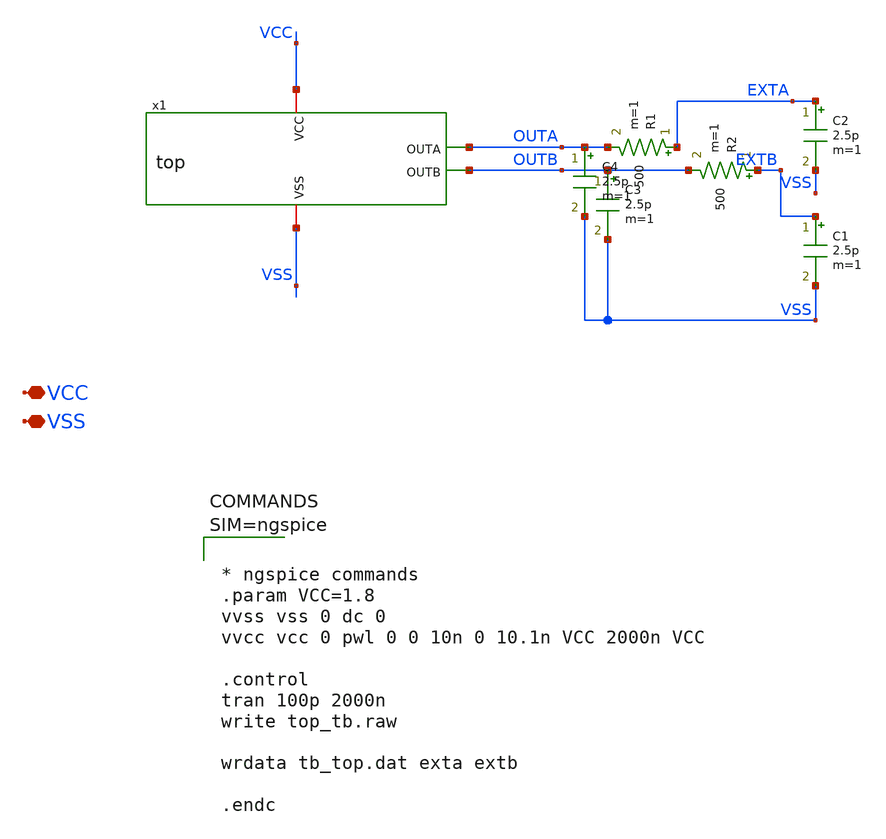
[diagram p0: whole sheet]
** sch_path: xschem/top_tb.sch
**.subckt top_tb VCC VSS
*.iopin VCC
*.iopin VSS
x1 VCC OUTA OUTB VSS top
R1 EXTA OUTA 500 m=1
R2 EXTB OUTB 500 m=1
C1 EXTB VSS 2.5p m=1
C2 EXTA VSS 2.5p m=1
C3 OUTB VSS 2.5p m=1
C4 OUTA VSS 2.5p m=1
**** begin user architecture code

** opencircuitdesign pdks install
.lib $::SKYWATER_MODELS/sky130.lib.spice tt





* ngspice commands
.param VCC=1.8
vvss vss 0 dc 0
vvcc vcc 0 pwl 0 0 10n 0 10.1n VCC 2000n VCC

.control
tran 100p 2000n
write top_tb.raw

wrdata tb_top.dat exta extb

.endc




**** end user architecture code
**.ends

* expanding   symbol:  top.sym # of pins=4
** sym_path: xschem/top.sym
** sch_path: xschem/top.sch
.subckt top VCC OUTA OUTB VSS
*.iopin VCC
*.iopin VSS
*.opin OUTA
*.opin OUTB
x1 VCC OSCA VSS oscillator_20MHZ
x2 VCC OSCB VSS oscillator_21MHZ
x5 VCC VSS IBIAS current_source
x6 VCC FIL_OUTA OSCA_BUF VSS IBIAS filter22M
x7 VCC FIL_OUTB OSCB_BUF VSS IBIAS filter22M
x10 VCC OSCA OSCA_BUF IBIAS VSS analog_buffer
x8 VCC OSCB OSCB_BUF IBIAS VSS analog_buffer
x9 VCC FIL_OUTA OUTA IBIAS VSS analog_buffer
x3 VCC FIL_OUTB OUTB IBIAS VSS analog_buffer
.ends


* expanding   symbol:  oscillator_20MHZ.sym # of pins=3
** sym_path: xschem/oscillator_20MHZ.sym
** sch_path: xschem/oscillator_20MHZ.sch
.subckt oscillator_20MHZ VCC OUT VSS
*.iopin VCC
*.iopin VSS
*.opin OUT
x1[30] INI[29] OUT_INI VCC VSS inverter
x1[29] INI[28] INI[29] VCC VSS inverter
x1[28] INI[27] INI[28] VCC VSS inverter
x1[27] INI[26] INI[27] VCC VSS inverter
x1[26] INI[25] INI[26] VCC VSS inverter
x1[25] INI[24] INI[25] VCC VSS inverter
x1[24] INI[23] INI[24] VCC VSS inverter
x1[23] INI[22] INI[23] VCC VSS inverter
x1[22] INI[21] INI[22] VCC VSS inverter
x1[21] INI[20] INI[21] VCC VSS inverter
x1[20] INI[19] INI[20] VCC VSS inverter
x1[19] INI[18] INI[19] VCC VSS inverter
x1[18] INI[17] INI[18] VCC VSS inverter
x1[17] INI[16] INI[17] VCC VSS inverter
x1[16] INI[15] INI[16] VCC VSS inverter
x1[15] INI[14] INI[15] VCC VSS inverter
x1[14] INI[13] INI[14] VCC VSS inverter
x1[13] INI[12] INI[13] VCC VSS inverter
x1[12] INI[11] INI[12] VCC VSS inverter
x1[11] INI[10] INI[11] VCC VSS inverter
x1[10] INI[9] INI[10] VCC VSS inverter
x1[9] INI[8] INI[9] VCC VSS inverter
x1[8] INI[7] INI[8] VCC VSS inverter
x1[7] INI[6] INI[7] VCC VSS inverter
x1[6] INI[5] INI[6] VCC VSS inverter
x1[5] INI[4] INI[5] VCC VSS inverter
x1[4] INI[3] INI[4] VCC VSS inverter
x1[3] INI[2] INI[3] VCC VSS inverter
x1[2] INI[1] INI[2] VCC VSS inverter
x1[1] INI[0] INI[1] VCC VSS inverter
x1[0] OUT_INI INI[0] VCC VSS inverter
x3 OUT OUT_INI VCC VSS inverter
.ends


* expanding   symbol:  oscillator_21MHZ.sym # of pins=3
** sym_path: xschem/oscillator_21MHZ.sym
** sch_path: xschem/oscillator_21MHZ.sch
.subckt oscillator_21MHZ VCC OUT VSS
*.iopin VCC
*.iopin VSS
*.opin OUT
x1[20] INI[19] OUT_INI VCC VSS inverter
x1[19] INI[18] INI[19] VCC VSS inverter
x1[18] INI[17] INI[18] VCC VSS inverter
x1[17] INI[16] INI[17] VCC VSS inverter
x1[16] INI[15] INI[16] VCC VSS inverter
x1[15] INI[14] INI[15] VCC VSS inverter
x1[14] INI[13] INI[14] VCC VSS inverter
x1[13] INI[12] INI[13] VCC VSS inverter
x1[12] INI[11] INI[12] VCC VSS inverter
x1[11] INI[10] INI[11] VCC VSS inverter
x1[10] INI[9] INI[10] VCC VSS inverter
x1[9] INI[8] INI[9] VCC VSS inverter
x1[8] INI[7] INI[8] VCC VSS inverter
x1[7] INI[6] INI[7] VCC VSS inverter
x1[6] INI[5] INI[6] VCC VSS inverter
x1[5] INI[4] INI[5] VCC VSS inverter
x1[4] INI[3] INI[4] VCC VSS inverter
x1[3] INI[2] INI[3] VCC VSS inverter
x1[2] INI[1] INI[2] VCC VSS inverter
x1[1] INI[0] INI[1] VCC VSS inverter
x1[0] OUT_INI INI[0] VCC VSS inverter
x1 OUT OUT_INI VCC VSS inverter
.ends


* expanding   symbol:  current_source.sym # of pins=3
** sym_path: xschem/current_source.sym
** sch_path: xschem/current_source.sch
.subckt current_source VCC VSS IBIAS
*.iopin VCC
*.iopin VSS
*.opin IBIAS
XM3 IBIAS IBIAS VSS VSS sky130_fd_pr__nfet_01v8 L=1 W=40 nf=1 ad='int((nf+1)/2) * W/nf * 0.29' as='int((nf+2)/2) * W/nf * 0.29'
+ pd='2*int((nf+1)/2) * (W/nf + 0.29)' ps='2*int((nf+2)/2) * (W/nf + 0.29)' nrd='0.29 / W' nrs='0.29 / W'
+ sa=0 sb=0 sd=0 mult=1 m=1
XR1 IBIAS VCC sky130_fd_pr__res_generic_po W=0.33 L=12 m=1
.ends


* expanding   symbol:  filter22M.sym # of pins=5
** sym_path: xschem/filter22M.sym
** sch_path: xschem/filter22M.sch
.subckt filter22M vcc fil_out fil_in vss IBIAS
*.opin fil_out
*.ipin fil_in
*.iopin vcc
*.iopin vss
*.ipin IBIAS
x1 VCC fil_out fil_out net1 VSS IBIAS opamp_1
XR1 fil_in mid sky130_fd_pr__res_generic_po W=0.5 L=100 m=1
XR2 mid net1 sky130_fd_pr__res_generic_po W=0.5 L=100 m=1
XC1 mid fil_out sky130_fd_pr__cap_mim_m3_2 W=10 L=12 MF=4 m=4
XC2 net1 VSS sky130_fd_pr__cap_mim_m3_2 W=10 L=6 MF=4 m=4
.ends


* expanding   symbol:  analog_buffer.sym # of pins=5
** sym_path: xschem/analog_buffer.sym
** sch_path: xschem/analog_buffer.sch
.subckt analog_buffer VCC BUF_IN BUF_OUT IBIAS VSS
*.ipin BUF_IN
*.iopin VCC
*.iopin VSS
*.ipin IBIAS
*.opin BUF_OUT
x8 VCC BUF_OUT BUF_OUT BUF_IN VSS IBIAS opamp_1
.ends


* expanding   symbol:  inverter.sym # of pins=4
** sym_path: xschem/inverter.sym
** sch_path: xschem/inverter.sch
.subckt inverter OUT IN VCC VSS
*.iopin VCC
*.iopin VSS
*.ipin IN
*.opin OUT
XM1 OUT IN net1 VCC sky130_fd_pr__pfet_01v8 L=1 W=2 nf=1 ad='int((nf+1)/2) * W/nf * 0.29' as='int((nf+2)/2) * W/nf * 0.29'
+ pd='2*int((nf+1)/2) * (W/nf + 0.29)' ps='2*int((nf+2)/2) * (W/nf + 0.29)' nrd='0.29 / W' nrs='0.29 / W'
+ sa=0 sb=0 sd=0 mult=1 m=1
XM2 OUT IN net2 VSS sky130_fd_pr__nfet_01v8 L=1 W=1 nf=1 ad='int((nf+1)/2) * W/nf * 0.29' as='int((nf+2)/2) * W/nf * 0.29'
+ pd='2*int((nf+1)/2) * (W/nf + 0.29)' ps='2*int((nf+2)/2) * (W/nf + 0.29)' nrd='0.29 / W' nrs='0.29 / W'
+ sa=0 sb=0 sd=0 mult=1 m=1
XM3 net1 VSS VCC VCC sky130_fd_pr__pfet_01v8 L=1 W=2 nf=1 ad='int((nf+1)/2) * W/nf * 0.29' as='int((nf+2)/2) * W/nf * 0.29'
+ pd='2*int((nf+1)/2) * (W/nf + 0.29)' ps='2*int((nf+2)/2) * (W/nf + 0.29)' nrd='0.29 / W' nrs='0.29 / W'
+ sa=0 sb=0 sd=0 mult=1 m=1
XM4 net2 VCC VSS VSS sky130_fd_pr__nfet_01v8 L=1 W=1 nf=1 ad='int((nf+1)/2) * W/nf * 0.29' as='int((nf+2)/2) * W/nf * 0.29'
+ pd='2*int((nf+1)/2) * (W/nf + 0.29)' ps='2*int((nf+2)/2) * (W/nf + 0.29)' nrd='0.29 / W' nrs='0.29 / W'
+ sa=0 sb=0 sd=0 mult=1 m=1
.ends


* expanding   symbol:  opamp_1.sym # of pins=6
** sym_path: xschem/opamp_1.sym
** sch_path: xschem/opamp_1.sch
.subckt opamp_1 VCC OUT INA INB VSS IBIAS
*.ipin INA
*.ipin INB
*.opin OUT
*.iopin VCC
*.iopin VSS
*.ipin IBIAS
XM1 MIRR INA TAILV VSS sky130_fd_pr__nfet_01v8 L=1 W=20 nf=1 ad='int((nf+1)/2) * W/nf * 0.29' as='int((nf+2)/2) * W/nf * 0.29'
+ pd='2*int((nf+1)/2) * (W/nf + 0.29)' ps='2*int((nf+2)/2) * (W/nf + 0.29)' nrd='0.29 / W' nrs='0.29 / W'
+ sa=0 sb=0 sd=0 mult=1 m=1
XM2 DIFF_OUT INB TAILV VSS sky130_fd_pr__nfet_01v8 L=1 W=20 nf=1 ad='int((nf+1)/2) * W/nf * 0.29' as='int((nf+2)/2) * W/nf * 0.29'
+ pd='2*int((nf+1)/2) * (W/nf + 0.29)' ps='2*int((nf+2)/2) * (W/nf + 0.29)' nrd='0.29 / W' nrs='0.29 / W'
+ sa=0 sb=0 sd=0 mult=1 m=1
XM3 TAILV IBIAS VSS VSS sky130_fd_pr__nfet_01v8 L=1 W=40 nf=1 ad='int((nf+1)/2) * W/nf * 0.29' as='int((nf+2)/2) * W/nf * 0.29'
+ pd='2*int((nf+1)/2) * (W/nf + 0.29)' ps='2*int((nf+2)/2) * (W/nf + 0.29)' nrd='0.29 / W' nrs='0.29 / W'
+ sa=0 sb=0 sd=0 mult=1 m=1
XM4 MIRR MIRR VCC VCC sky130_fd_pr__pfet_01v8_lvt L=0.5 W=14 nf=1 ad='int((nf+1)/2) * W/nf * 0.29' as='int((nf+2)/2) * W/nf * 0.29'
+ pd='2*int((nf+1)/2) * (W/nf + 0.29)' ps='2*int((nf+2)/2) * (W/nf + 0.29)' nrd='0.29 / W' nrs='0.29 / W'
+ sa=0 sb=0 sd=0 mult=1 m=1
XM5 DIFF_OUT MIRR VCC VCC sky130_fd_pr__pfet_01v8_lvt L=0.5 W=14 nf=1 ad='int((nf+1)/2) * W/nf * 0.29'
+ as='int((nf+2)/2) * W/nf * 0.29' pd='2*int((nf+1)/2) * (W/nf + 0.29)' ps='2*int((nf+2)/2) * (W/nf + 0.29)'
+ nrd='0.29 / W' nrs='0.29 / W' sa=0 sb=0 sd=0 mult=1 m=1
XM6 OUT IBIAS VSS VSS sky130_fd_pr__nfet_01v8 L=0.5 W=93 nf=1 ad='int((nf+1)/2) * W/nf * 0.29' as='int((nf+2)/2) * W/nf * 0.29'
+ pd='2*int((nf+1)/2) * (W/nf + 0.29)' ps='2*int((nf+2)/2) * (W/nf + 0.29)' nrd='0.29 / W' nrs='0.29 / W'
+ sa=0 sb=0 sd=0 mult=1 m=1
XM7 OUT DIFF_OUT VCC VCC sky130_fd_pr__pfet_01v8_lvt L=0.5 W=70 nf=1 ad='int((nf+1)/2) * W/nf * 0.29'
+ as='int((nf+2)/2) * W/nf * 0.29' pd='2*int((nf+1)/2) * (W/nf + 0.29)' ps='2*int((nf+2)/2) * (W/nf + 0.29)'
+ nrd='0.29 / W' nrs='0.29 / W' sa=0 sb=0 sd=0 mult=1 m=1
XM9 RBIAS IBIAS VSS VSS sky130_fd_pr__nfet_01v8 L=1 W=5 nf=1 ad='int((nf+1)/2) * W/nf * 0.29' as='int((nf+2)/2) * W/nf * 0.29'
+ pd='2*int((nf+1)/2) * (W/nf + 0.29)' ps='2*int((nf+2)/2) * (W/nf + 0.29)' nrd='0.29 / W' nrs='0.29 / W'
+ sa=0 sb=0 sd=0 mult=1 m=1
XM10 RBIAS RBIAS net2 VCC sky130_fd_pr__pfet_01v8_lvt L=0.5 W=1 nf=1 ad='int((nf+1)/2) * W/nf * 0.29'
+ as='int((nf+2)/2) * W/nf * 0.29' pd='2*int((nf+1)/2) * (W/nf + 0.29)' ps='2*int((nf+2)/2) * (W/nf + 0.29)'
+ nrd='0.29 / W' nrs='0.29 / W' sa=0 sb=0 sd=0 mult=1 m=1
XM11 net2 net2 VCC VCC sky130_fd_pr__pfet_01v8_lvt L=0.5 W=7.5 nf=1 ad='int((nf+1)/2) * W/nf * 0.29'
+ as='int((nf+2)/2) * W/nf * 0.29' pd='2*int((nf+1)/2) * (W/nf + 0.29)' ps='2*int((nf+2)/2) * (W/nf + 0.29)'
+ nrd='0.29 / W' nrs='0.29 / W' sa=0 sb=0 sd=0 mult=1 m=1
XC1 OUT net1 sky130_fd_pr__cap_mim_m3_2 W=20 L=13 MF=1 m=1
XM8 net1 RBIAS DIFF_OUT VCC sky130_fd_pr__pfet_01v8_lvt L=0.5 W=14 nf=1 ad='int((nf+1)/2) * W/nf * 0.29'
+ as='int((nf+2)/2) * W/nf * 0.29' pd='2*int((nf+1)/2) * (W/nf + 0.29)' ps='2*int((nf+2)/2) * (W/nf + 0.29)'
+ nrd='0.29 / W' nrs='0.29 / W' sa=0 sb=0 sd=0 mult=1 m=1
.ends

.end
